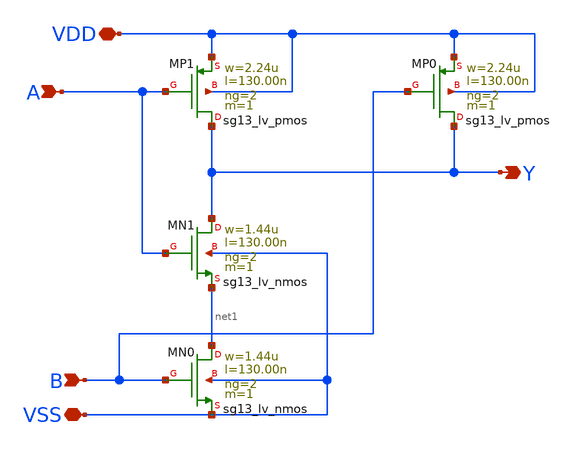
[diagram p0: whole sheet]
** sch_path: current_generator/analog/DAC/schematics/nand.sch
**.subckt nand Y A VDD VSS B
*.opin Y
*.ipin A
*.iopin VDD
*.iopin VSS
*.ipin B
XMN0 net1 B VSS VSS sg13_lv_nmos w=1.44u l=130.00n ng=2 m=1 mm_ok=1
XMP0 Y B VDD VDD sg13_lv_pmos w=2.24u l=130.00n ng=2 m=1 mm_ok=1
XMN1 Y A net1 VSS sg13_lv_nmos w=1.44u l=130.00n ng=2 m=1 mm_ok=1
XMP1 Y A VDD VDD sg13_lv_pmos w=2.24u l=130.00n ng=2 m=1 mm_ok=1
**.ends
.end
